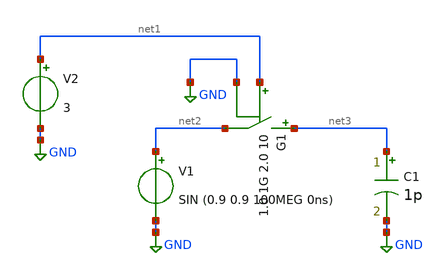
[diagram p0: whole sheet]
** sch_path: SampleHold/ideal_switch.sch
**.subckt ideal_switch
G1 net3 net2 vcr pwl(1) net1 GND 1.0 1G 2.0 10
C1 net3 GND 1p m=1
V1 net2 GND SIN (0.9 0.9 100MEG 0ns)
V2 net1 GND 3
**.ends
.GLOBAL GND
.end
